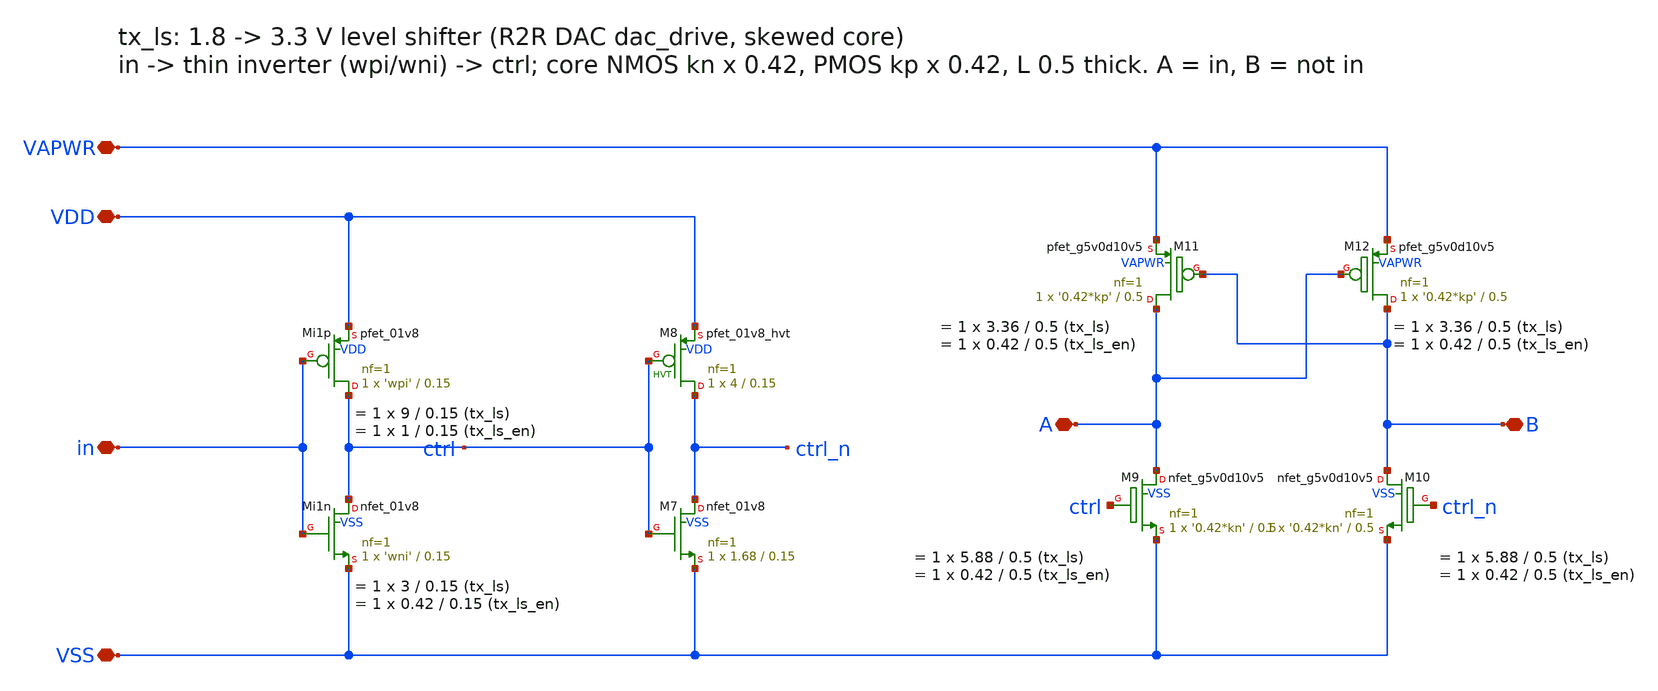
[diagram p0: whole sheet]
** sch_path: xschem/tx_ls.sch
**.subckt tx_ls VDD VAPWR VSS in A B
*.iopin VDD
*.iopin VAPWR
*.iopin VSS
*.iopin in
*.iopin A
*.iopin B
XMi1p ctrl in VDD VDD sky130_fd_pr__pfet_01v8 L=0.15 W='wpi' nf=1 ad='int((nf+1)/2) * W/nf * 0.29' as='int((nf+2)/2) * W/nf * 0.29'
+ pd='2*int((nf+1)/2) * (W/nf + 0.29)' ps='2*int((nf+2)/2) * (W/nf + 0.29)' nrd='0.29 / W' nrs='0.29 / W'
+ sa=0 sb=0 sd=0 mult=1 m=1
XMi1n ctrl in VSS VSS sky130_fd_pr__nfet_01v8 L=0.15 W='wni' nf=1 ad='int((nf+1)/2) * W/nf * 0.29' as='int((nf+2)/2) * W/nf * 0.29'
+ pd='2*int((nf+1)/2) * (W/nf + 0.29)' ps='2*int((nf+2)/2) * (W/nf + 0.29)' nrd='0.29 / W' nrs='0.29 / W'
+ sa=0 sb=0 sd=0 mult=1 m=1
XM8 ctrl_n ctrl VDD VDD sky130_fd_pr__pfet_01v8_hvt L=0.15 W=4 nf=1 ad='int((nf+1)/2) * W/nf * 0.29'
+ as='int((nf+2)/2) * W/nf * 0.29' pd='2*int((nf+1)/2) * (W/nf + 0.29)' ps='2*int((nf+2)/2) * (W/nf + 0.29)'
+ nrd='0.29 / W' nrs='0.29 / W' sa=0 sb=0 sd=0 mult=1 m=1
XM7 ctrl_n ctrl VSS VSS sky130_fd_pr__nfet_01v8 L=0.15 W=1.68 nf=1 ad='int((nf+1)/2) * W/nf * 0.29' as='int((nf+2)/2) * W/nf * 0.29'
+ pd='2*int((nf+1)/2) * (W/nf + 0.29)' ps='2*int((nf+2)/2) * (W/nf + 0.29)' nrd='0.29 / W' nrs='0.29 / W'
+ sa=0 sb=0 sd=0 mult=1 m=1
XM9 A ctrl VSS VSS sky130_fd_pr__nfet_g5v0d10v5 L=0.5 W='0.42*kn' nf=1 ad='int((nf+1)/2) * W/nf * 0.29'
+ as='int((nf+2)/2) * W/nf * 0.29' pd='2*int((nf+1)/2) * (W/nf + 0.29)' ps='2*int((nf+2)/2) * (W/nf + 0.29)'
+ nrd='0.29 / W' nrs='0.29 / W' sa=0 sb=0 sd=0 mult=1 m=1
XM10 B ctrl_n VSS VSS sky130_fd_pr__nfet_g5v0d10v5 L=0.5 W='0.42*kn' nf=1 ad='int((nf+1)/2) * W/nf * 0.29'
+ as='int((nf+2)/2) * W/nf * 0.29' pd='2*int((nf+1)/2) * (W/nf + 0.29)' ps='2*int((nf+2)/2) * (W/nf + 0.29)'
+ nrd='0.29 / W' nrs='0.29 / W' sa=0 sb=0 sd=0 mult=1 m=1
XM11 A B VAPWR VAPWR sky130_fd_pr__pfet_g5v0d10v5 L=0.5 W='0.42*kp' nf=1 ad='int((nf+1)/2) * W/nf * 0.29'
+ as='int((nf+2)/2) * W/nf * 0.29' pd='2*int((nf+1)/2) * (W/nf + 0.29)' ps='2*int((nf+2)/2) * (W/nf + 0.29)'
+ nrd='0.29 / W' nrs='0.29 / W' sa=0 sb=0 sd=0 mult=1 m=1
XM12 B A VAPWR VAPWR sky130_fd_pr__pfet_g5v0d10v5 L=0.5 W='0.42*kp' nf=1 ad='int((nf+1)/2) * W/nf * 0.29'
+ as='int((nf+2)/2) * W/nf * 0.29' pd='2*int((nf+1)/2) * (W/nf + 0.29)' ps='2*int((nf+2)/2) * (W/nf + 0.29)'
+ nrd='0.29 / W' nrs='0.29 / W' sa=0 sb=0 sd=0 mult=1 m=1
**.ends
.end
